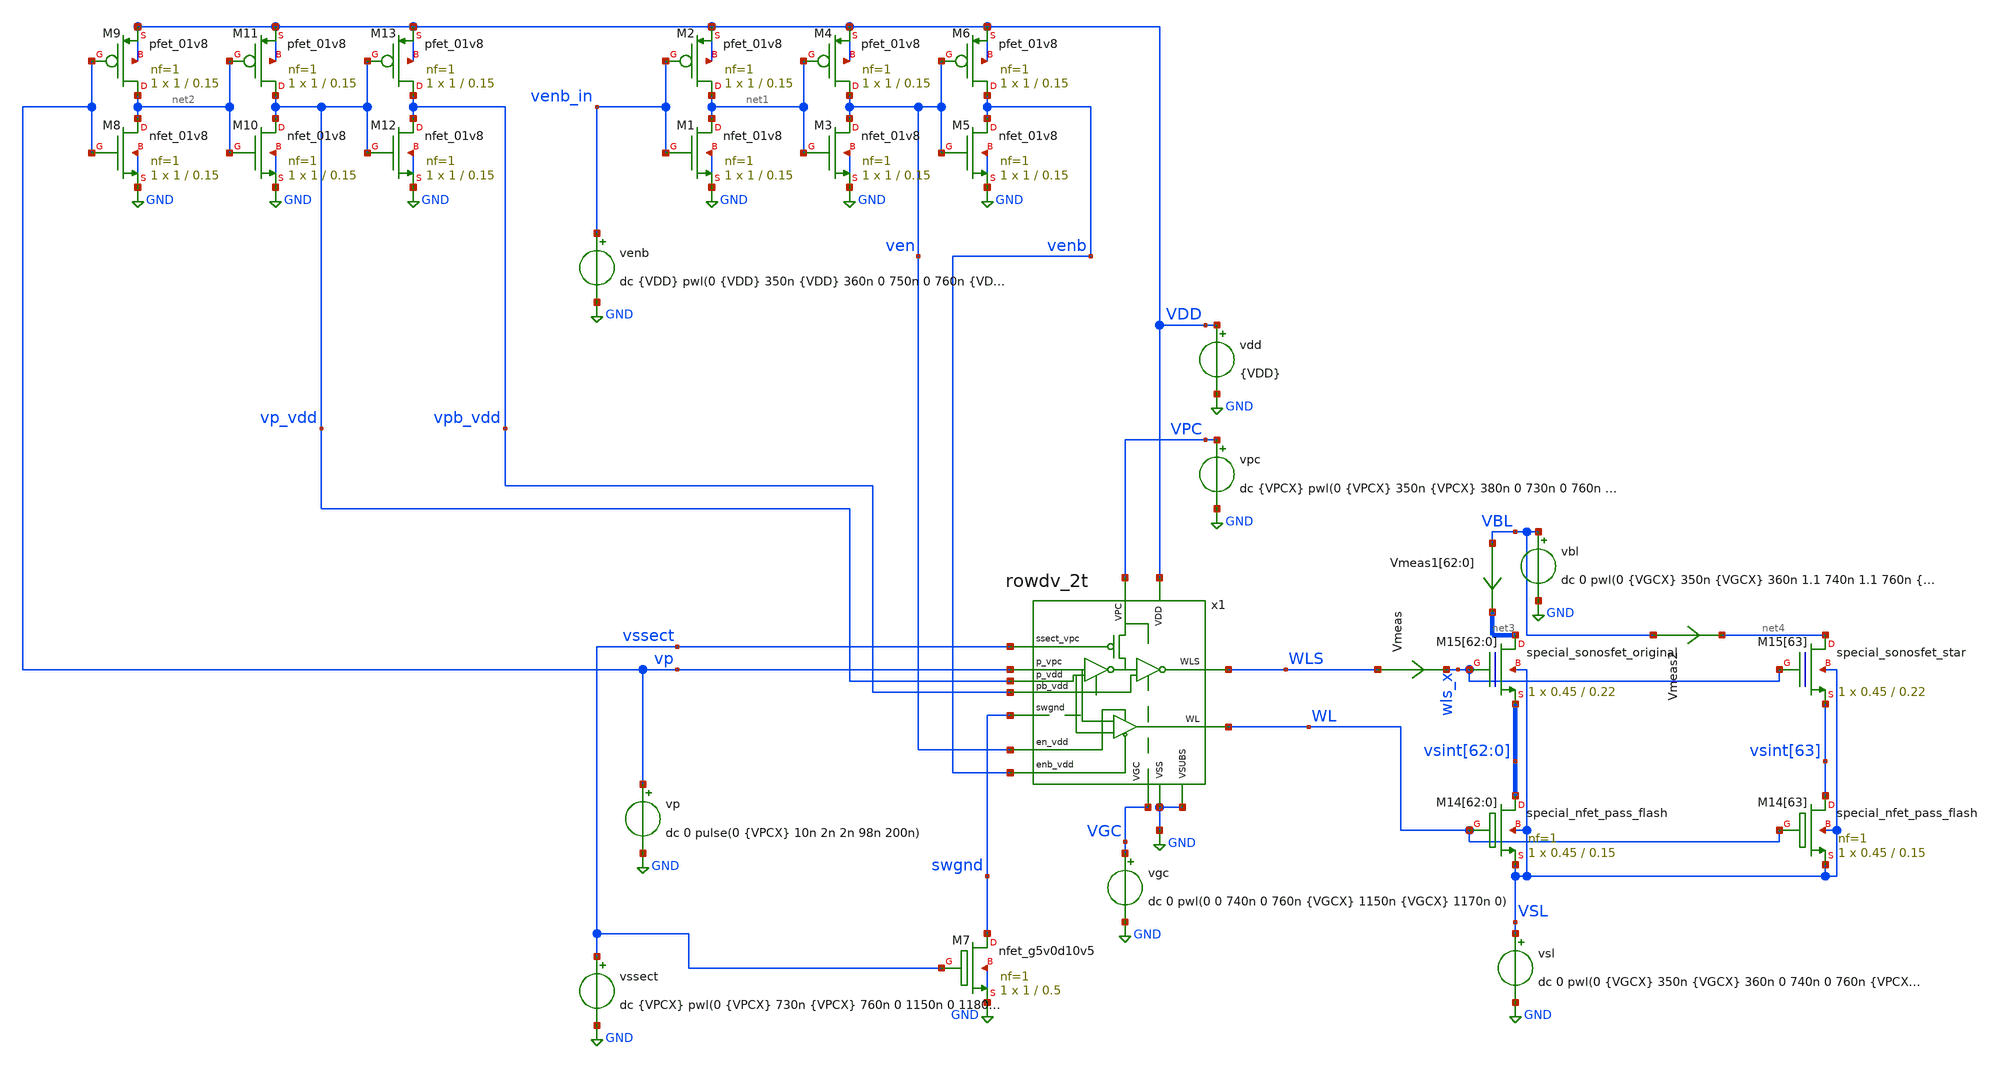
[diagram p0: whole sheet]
** sch_path: integrated/rowdv_2t_sonos/test_rowdv_2t.sch
**.subckt test_rowdv_2t
vssect vssect GND dc {VPCX} pwl(0 {VPCX} 730n {VPCX} 760n 0 1150n 0 1180n {VPCX})
vp vp GND dc 0 pulse(0 {VPCX} 10n 2n 2n 98n 200n)
venb venb_in GND dc {VDD} pwl(0 {VDD} 350n {VDD} 360n 0 750n 0 760n {VDD} 1170n {VDD} 1180n 0)
XM1 net1 venb_in GND GND sky130_fd_pr__nfet_01v8 L=0.15 W=1 nf=1 ad='int((nf+1)/2) * W/nf * 0.29' as='int((nf+2)/2) * W/nf * 0.29'
+ pd='2*int((nf+1)/2) * (W/nf + 0.29)' ps='2*int((nf+2)/2) * (W/nf + 0.29)' nrd='0.29 / W' nrs='0.29 / W'
+ sa=0 sb=0 sd=0 mult=1 m=1
XM2 net1 venb_in VDD VDD sky130_fd_pr__pfet_01v8 L=0.15 W=1 nf=1 ad='int((nf+1)/2) * W/nf * 0.29' as='int((nf+2)/2) * W/nf * 0.29'
+ pd='2*int((nf+1)/2) * (W/nf + 0.29)' ps='2*int((nf+2)/2) * (W/nf + 0.29)' nrd='0.29 / W' nrs='0.29 / W'
+ sa=0 sb=0 sd=0 mult=1 m=1
vpc VPC GND dc {VPCX} pwl(0 {VPCX} 350n {VPCX} 380n 0 730n 0 760n {VDD} 1140n {VDD} 1170n 0)
vdd VDD GND {VDD}
vgc VGC GND dc 0 pwl(0 0 740n 0 760n {VGCX} 1150n {VGCX} 1170n 0)
XM3 ven net1 GND GND sky130_fd_pr__nfet_01v8 L=0.15 W=1 nf=1 ad='int((nf+1)/2) * W/nf * 0.29' as='int((nf+2)/2) * W/nf * 0.29'
+ pd='2*int((nf+1)/2) * (W/nf + 0.29)' ps='2*int((nf+2)/2) * (W/nf + 0.29)' nrd='0.29 / W' nrs='0.29 / W'
+ sa=0 sb=0 sd=0 mult=1 m=1
XM4 ven net1 VDD VDD sky130_fd_pr__pfet_01v8 L=0.15 W=1 nf=1 ad='int((nf+1)/2) * W/nf * 0.29' as='int((nf+2)/2) * W/nf * 0.29'
+ pd='2*int((nf+1)/2) * (W/nf + 0.29)' ps='2*int((nf+2)/2) * (W/nf + 0.29)' nrd='0.29 / W' nrs='0.29 / W'
+ sa=0 sb=0 sd=0 mult=1 m=1
XM5 venb ven GND GND sky130_fd_pr__nfet_01v8 L=0.15 W=1 nf=1 ad='int((nf+1)/2) * W/nf * 0.29' as='int((nf+2)/2) * W/nf * 0.29'
+ pd='2*int((nf+1)/2) * (W/nf + 0.29)' ps='2*int((nf+2)/2) * (W/nf + 0.29)' nrd='0.29 / W' nrs='0.29 / W'
+ sa=0 sb=0 sd=0 mult=1 m=1
XM6 venb ven VDD VDD sky130_fd_pr__pfet_01v8 L=0.15 W=1 nf=1 ad='int((nf+1)/2) * W/nf * 0.29' as='int((nf+2)/2) * W/nf * 0.29'
+ pd='2*int((nf+1)/2) * (W/nf + 0.29)' ps='2*int((nf+2)/2) * (W/nf + 0.29)' nrd='0.29 / W' nrs='0.29 / W'
+ sa=0 sb=0 sd=0 mult=1 m=1
XM7 swgnd vssect GND GND sky130_fd_pr__nfet_g5v0d10v5 L=0.5 W=1 nf=1 ad='int((nf+1)/2) * W/nf * 0.29'
+ as='int((nf+2)/2) * W/nf * 0.29' pd='2*int((nf+1)/2) * (W/nf + 0.29)' ps='2*int((nf+2)/2) * (W/nf + 0.29)'
+ nrd='0.29 / W' nrs='0.29 / W' sa=0 sb=0 sd=0 mult=1 m=1
x1 vssect ven venb vp vp_vdd vpb_vdd swgnd VPC VGC VDD GND GND WLS WL rowdv_2t
XM8 net2 vp GND GND sky130_fd_pr__nfet_01v8 L=0.15 W=1 nf=1 ad='int((nf+1)/2) * W/nf * 0.29' as='int((nf+2)/2) * W/nf * 0.29'
+ pd='2*int((nf+1)/2) * (W/nf + 0.29)' ps='2*int((nf+2)/2) * (W/nf + 0.29)' nrd='0.29 / W' nrs='0.29 / W'
+ sa=0 sb=0 sd=0 mult=1 m=1
XM9 net2 vp VDD VDD sky130_fd_pr__pfet_01v8 L=0.15 W=1 nf=1 ad='int((nf+1)/2) * W/nf * 0.29' as='int((nf+2)/2) * W/nf * 0.29'
+ pd='2*int((nf+1)/2) * (W/nf + 0.29)' ps='2*int((nf+2)/2) * (W/nf + 0.29)' nrd='0.29 / W' nrs='0.29 / W'
+ sa=0 sb=0 sd=0 mult=1 m=1
XM10 vp_vdd net2 GND GND sky130_fd_pr__nfet_01v8 L=0.15 W=1 nf=1 ad='int((nf+1)/2) * W/nf * 0.29' as='int((nf+2)/2) * W/nf * 0.29'
+ pd='2*int((nf+1)/2) * (W/nf + 0.29)' ps='2*int((nf+2)/2) * (W/nf + 0.29)' nrd='0.29 / W' nrs='0.29 / W'
+ sa=0 sb=0 sd=0 mult=1 m=1
XM11 vp_vdd net2 VDD VDD sky130_fd_pr__pfet_01v8 L=0.15 W=1 nf=1 ad='int((nf+1)/2) * W/nf * 0.29' as='int((nf+2)/2) * W/nf * 0.29'
+ pd='2*int((nf+1)/2) * (W/nf + 0.29)' ps='2*int((nf+2)/2) * (W/nf + 0.29)' nrd='0.29 / W' nrs='0.29 / W'
+ sa=0 sb=0 sd=0 mult=1 m=1
XM12 vpb_vdd vp_vdd GND GND sky130_fd_pr__nfet_01v8 L=0.15 W=1 nf=1 ad='int((nf+1)/2) * W/nf * 0.29'
+ as='int((nf+2)/2) * W/nf * 0.29' pd='2*int((nf+1)/2) * (W/nf + 0.29)' ps='2*int((nf+2)/2) * (W/nf + 0.29)'
+ nrd='0.29 / W' nrs='0.29 / W' sa=0 sb=0 sd=0 mult=1 m=1
XM13 vpb_vdd vp_vdd VDD VDD sky130_fd_pr__pfet_01v8 L=0.15 W=1 nf=1 ad='int((nf+1)/2) * W/nf * 0.29'
+ as='int((nf+2)/2) * W/nf * 0.29' pd='2*int((nf+1)/2) * (W/nf + 0.29)' ps='2*int((nf+2)/2) * (W/nf + 0.29)'
+ nrd='0.29 / W' nrs='0.29 / W' sa=0 sb=0 sd=0 mult=1 m=1
XM15[62] net3[62] wls_x vsint[62] VSL sky130_fd_bs_flash__special_sonosfet_original L=0.22 W=0.45 nf=1
+ ad='1 * W * 0.29' as='1 * W * 0.29' pd='2 * (W + 0.29)' ps='2 * (W + 0.29)' nrd='0.29 / W' nrs='0.29 / W'
+ sa=0 sb=0 sd=0 mult=1 m=1
XM15[61] net3[61] wls_x vsint[61] VSL sky130_fd_bs_flash__special_sonosfet_original L=0.22 W=0.45 nf=1
+ ad='1 * W * 0.29' as='1 * W * 0.29' pd='2 * (W + 0.29)' ps='2 * (W + 0.29)' nrd='0.29 / W' nrs='0.29 / W'
+ sa=0 sb=0 sd=0 mult=1 m=1
XM15[60] net3[60] wls_x vsint[60] VSL sky130_fd_bs_flash__special_sonosfet_original L=0.22 W=0.45 nf=1
+ ad='1 * W * 0.29' as='1 * W * 0.29' pd='2 * (W + 0.29)' ps='2 * (W + 0.29)' nrd='0.29 / W' nrs='0.29 / W'
+ sa=0 sb=0 sd=0 mult=1 m=1
XM15[59] net3[59] wls_x vsint[59] VSL sky130_fd_bs_flash__special_sonosfet_original L=0.22 W=0.45 nf=1
+ ad='1 * W * 0.29' as='1 * W * 0.29' pd='2 * (W + 0.29)' ps='2 * (W + 0.29)' nrd='0.29 / W' nrs='0.29 / W'
+ sa=0 sb=0 sd=0 mult=1 m=1
XM15[58] net3[58] wls_x vsint[58] VSL sky130_fd_bs_flash__special_sonosfet_original L=0.22 W=0.45 nf=1
+ ad='1 * W * 0.29' as='1 * W * 0.29' pd='2 * (W + 0.29)' ps='2 * (W + 0.29)' nrd='0.29 / W' nrs='0.29 / W'
+ sa=0 sb=0 sd=0 mult=1 m=1
XM15[57] net3[57] wls_x vsint[57] VSL sky130_fd_bs_flash__special_sonosfet_original L=0.22 W=0.45 nf=1
+ ad='1 * W * 0.29' as='1 * W * 0.29' pd='2 * (W + 0.29)' ps='2 * (W + 0.29)' nrd='0.29 / W' nrs='0.29 / W'
+ sa=0 sb=0 sd=0 mult=1 m=1
XM15[56] net3[56] wls_x vsint[56] VSL sky130_fd_bs_flash__special_sonosfet_original L=0.22 W=0.45 nf=1
+ ad='1 * W * 0.29' as='1 * W * 0.29' pd='2 * (W + 0.29)' ps='2 * (W + 0.29)' nrd='0.29 / W' nrs='0.29 / W'
+ sa=0 sb=0 sd=0 mult=1 m=1
XM15[55] net3[55] wls_x vsint[55] VSL sky130_fd_bs_flash__special_sonosfet_original L=0.22 W=0.45 nf=1
+ ad='1 * W * 0.29' as='1 * W * 0.29' pd='2 * (W + 0.29)' ps='2 * (W + 0.29)' nrd='0.29 / W' nrs='0.29 / W'
+ sa=0 sb=0 sd=0 mult=1 m=1
XM15[54] net3[54] wls_x vsint[54] VSL sky130_fd_bs_flash__special_sonosfet_original L=0.22 W=0.45 nf=1
+ ad='1 * W * 0.29' as='1 * W * 0.29' pd='2 * (W + 0.29)' ps='2 * (W + 0.29)' nrd='0.29 / W' nrs='0.29 / W'
+ sa=0 sb=0 sd=0 mult=1 m=1
XM15[53] net3[53] wls_x vsint[53] VSL sky130_fd_bs_flash__special_sonosfet_original L=0.22 W=0.45 nf=1
+ ad='1 * W * 0.29' as='1 * W * 0.29' pd='2 * (W + 0.29)' ps='2 * (W + 0.29)' nrd='0.29 / W' nrs='0.29 / W'
+ sa=0 sb=0 sd=0 mult=1 m=1
XM15[52] net3[52] wls_x vsint[52] VSL sky130_fd_bs_flash__special_sonosfet_original L=0.22 W=0.45 nf=1
+ ad='1 * W * 0.29' as='1 * W * 0.29' pd='2 * (W + 0.29)' ps='2 * (W + 0.29)' nrd='0.29 / W' nrs='0.29 / W'
+ sa=0 sb=0 sd=0 mult=1 m=1
XM15[51] net3[51] wls_x vsint[51] VSL sky130_fd_bs_flash__special_sonosfet_original L=0.22 W=0.45 nf=1
+ ad='1 * W * 0.29' as='1 * W * 0.29' pd='2 * (W + 0.29)' ps='2 * (W + 0.29)' nrd='0.29 / W' nrs='0.29 / W'
+ sa=0 sb=0 sd=0 mult=1 m=1
XM15[50] net3[50] wls_x vsint[50] VSL sky130_fd_bs_flash__special_sonosfet_original L=0.22 W=0.45 nf=1
+ ad='1 * W * 0.29' as='1 * W * 0.29' pd='2 * (W + 0.29)' ps='2 * (W + 0.29)' nrd='0.29 / W' nrs='0.29 / W'
+ sa=0 sb=0 sd=0 mult=1 m=1
XM15[49] net3[49] wls_x vsint[49] VSL sky130_fd_bs_flash__special_sonosfet_original L=0.22 W=0.45 nf=1
+ ad='1 * W * 0.29' as='1 * W * 0.29' pd='2 * (W + 0.29)' ps='2 * (W + 0.29)' nrd='0.29 / W' nrs='0.29 / W'
+ sa=0 sb=0 sd=0 mult=1 m=1
XM15[48] net3[48] wls_x vsint[48] VSL sky130_fd_bs_flash__special_sonosfet_original L=0.22 W=0.45 nf=1
+ ad='1 * W * 0.29' as='1 * W * 0.29' pd='2 * (W + 0.29)' ps='2 * (W + 0.29)' nrd='0.29 / W' nrs='0.29 / W'
+ sa=0 sb=0 sd=0 mult=1 m=1
XM15[47] net3[47] wls_x vsint[47] VSL sky130_fd_bs_flash__special_sonosfet_original L=0.22 W=0.45 nf=1
+ ad='1 * W * 0.29' as='1 * W * 0.29' pd='2 * (W + 0.29)' ps='2 * (W + 0.29)' nrd='0.29 / W' nrs='0.29 / W'
+ sa=0 sb=0 sd=0 mult=1 m=1
XM15[46] net3[46] wls_x vsint[46] VSL sky130_fd_bs_flash__special_sonosfet_original L=0.22 W=0.45 nf=1
+ ad='1 * W * 0.29' as='1 * W * 0.29' pd='2 * (W + 0.29)' ps='2 * (W + 0.29)' nrd='0.29 / W' nrs='0.29 / W'
+ sa=0 sb=0 sd=0 mult=1 m=1
XM15[45] net3[45] wls_x vsint[45] VSL sky130_fd_bs_flash__special_sonosfet_original L=0.22 W=0.45 nf=1
+ ad='1 * W * 0.29' as='1 * W * 0.29' pd='2 * (W + 0.29)' ps='2 * (W + 0.29)' nrd='0.29 / W' nrs='0.29 / W'
+ sa=0 sb=0 sd=0 mult=1 m=1
XM15[44] net3[44] wls_x vsint[44] VSL sky130_fd_bs_flash__special_sonosfet_original L=0.22 W=0.45 nf=1
+ ad='1 * W * 0.29' as='1 * W * 0.29' pd='2 * (W + 0.29)' ps='2 * (W + 0.29)' nrd='0.29 / W' nrs='0.29 / W'
+ sa=0 sb=0 sd=0 mult=1 m=1
XM15[43] net3[43] wls_x vsint[43] VSL sky130_fd_bs_flash__special_sonosfet_original L=0.22 W=0.45 nf=1
+ ad='1 * W * 0.29' as='1 * W * 0.29' pd='2 * (W + 0.29)' ps='2 * (W + 0.29)' nrd='0.29 / W' nrs='0.29 / W'
+ sa=0 sb=0 sd=0 mult=1 m=1
XM15[42] net3[42] wls_x vsint[42] VSL sky130_fd_bs_flash__special_sonosfet_original L=0.22 W=0.45 nf=1
+ ad='1 * W * 0.29' as='1 * W * 0.29' pd='2 * (W + 0.29)' ps='2 * (W + 0.29)' nrd='0.29 / W' nrs='0.29 / W'
+ sa=0 sb=0 sd=0 mult=1 m=1
XM15[41] net3[41] wls_x vsint[41] VSL sky130_fd_bs_flash__special_sonosfet_original L=0.22 W=0.45 nf=1
+ ad='1 * W * 0.29' as='1 * W * 0.29' pd='2 * (W + 0.29)' ps='2 * (W + 0.29)' nrd='0.29 / W' nrs='0.29 / W'
+ sa=0 sb=0 sd=0 mult=1 m=1
XM15[40] net3[40] wls_x vsint[40] VSL sky130_fd_bs_flash__special_sonosfet_original L=0.22 W=0.45 nf=1
+ ad='1 * W * 0.29' as='1 * W * 0.29' pd='2 * (W + 0.29)' ps='2 * (W + 0.29)' nrd='0.29 / W' nrs='0.29 / W'
+ sa=0 sb=0 sd=0 mult=1 m=1
XM15[39] net3[39] wls_x vsint[39] VSL sky130_fd_bs_flash__special_sonosfet_original L=0.22 W=0.45 nf=1
+ ad='1 * W * 0.29' as='1 * W * 0.29' pd='2 * (W + 0.29)' ps='2 * (W + 0.29)' nrd='0.29 / W' nrs='0.29 / W'
+ sa=0 sb=0 sd=0 mult=1 m=1
XM15[38] net3[38] wls_x vsint[38] VSL sky130_fd_bs_flash__special_sonosfet_original L=0.22 W=0.45 nf=1
+ ad='1 * W * 0.29' as='1 * W * 0.29' pd='2 * (W + 0.29)' ps='2 * (W + 0.29)' nrd='0.29 / W' nrs='0.29 / W'
+ sa=0 sb=0 sd=0 mult=1 m=1
XM15[37] net3[37] wls_x vsint[37] VSL sky130_fd_bs_flash__special_sonosfet_original L=0.22 W=0.45 nf=1
+ ad='1 * W * 0.29' as='1 * W * 0.29' pd='2 * (W + 0.29)' ps='2 * (W + 0.29)' nrd='0.29 / W' nrs='0.29 / W'
+ sa=0 sb=0 sd=0 mult=1 m=1
XM15[36] net3[36] wls_x vsint[36] VSL sky130_fd_bs_flash__special_sonosfet_original L=0.22 W=0.45 nf=1
+ ad='1 * W * 0.29' as='1 * W * 0.29' pd='2 * (W + 0.29)' ps='2 * (W + 0.29)' nrd='0.29 / W' nrs='0.29 / W'
+ sa=0 sb=0 sd=0 mult=1 m=1
XM15[35] net3[35] wls_x vsint[35] VSL sky130_fd_bs_flash__special_sonosfet_original L=0.22 W=0.45 nf=1
+ ad='1 * W * 0.29' as='1 * W * 0.29' pd='2 * (W + 0.29)' ps='2 * (W + 0.29)' nrd='0.29 / W' nrs='0.29 / W'
+ sa=0 sb=0 sd=0 mult=1 m=1
XM15[34] net3[34] wls_x vsint[34] VSL sky130_fd_bs_flash__special_sonosfet_original L=0.22 W=0.45 nf=1
+ ad='1 * W * 0.29' as='1 * W * 0.29' pd='2 * (W + 0.29)' ps='2 * (W + 0.29)' nrd='0.29 / W' nrs='0.29 / W'
+ sa=0 sb=0 sd=0 mult=1 m=1
XM15[33] net3[33] wls_x vsint[33] VSL sky130_fd_bs_flash__special_sonosfet_original L=0.22 W=0.45 nf=1
+ ad='1 * W * 0.29' as='1 * W * 0.29' pd='2 * (W + 0.29)' ps='2 * (W + 0.29)' nrd='0.29 / W' nrs='0.29 / W'
+ sa=0 sb=0 sd=0 mult=1 m=1
XM15[32] net3[32] wls_x vsint[32] VSL sky130_fd_bs_flash__special_sonosfet_original L=0.22 W=0.45 nf=1
+ ad='1 * W * 0.29' as='1 * W * 0.29' pd='2 * (W + 0.29)' ps='2 * (W + 0.29)' nrd='0.29 / W' nrs='0.29 / W'
+ sa=0 sb=0 sd=0 mult=1 m=1
XM15[31] net3[31] wls_x vsint[31] VSL sky130_fd_bs_flash__special_sonosfet_original L=0.22 W=0.45 nf=1
+ ad='1 * W * 0.29' as='1 * W * 0.29' pd='2 * (W + 0.29)' ps='2 * (W + 0.29)' nrd='0.29 / W' nrs='0.29 / W'
+ sa=0 sb=0 sd=0 mult=1 m=1
XM15[30] net3[30] wls_x vsint[30] VSL sky130_fd_bs_flash__special_sonosfet_original L=0.22 W=0.45 nf=1
+ ad='1 * W * 0.29' as='1 * W * 0.29' pd='2 * (W + 0.29)' ps='2 * (W + 0.29)' nrd='0.29 / W' nrs='0.29 / W'
+ sa=0 sb=0 sd=0 mult=1 m=1
XM15[29] net3[29] wls_x vsint[29] VSL sky130_fd_bs_flash__special_sonosfet_original L=0.22 W=0.45 nf=1
+ ad='1 * W * 0.29' as='1 * W * 0.29' pd='2 * (W + 0.29)' ps='2 * (W + 0.29)' nrd='0.29 / W' nrs='0.29 / W'
+ sa=0 sb=0 sd=0 mult=1 m=1
XM15[28] net3[28] wls_x vsint[28] VSL sky130_fd_bs_flash__special_sonosfet_original L=0.22 W=0.45 nf=1
+ ad='1 * W * 0.29' as='1 * W * 0.29' pd='2 * (W + 0.29)' ps='2 * (W + 0.29)' nrd='0.29 / W' nrs='0.29 / W'
+ sa=0 sb=0 sd=0 mult=1 m=1
XM15[27] net3[27] wls_x vsint[27] VSL sky130_fd_bs_flash__special_sonosfet_original L=0.22 W=0.45 nf=1
+ ad='1 * W * 0.29' as='1 * W * 0.29' pd='2 * (W + 0.29)' ps='2 * (W + 0.29)' nrd='0.29 / W' nrs='0.29 / W'
+ sa=0 sb=0 sd=0 mult=1 m=1
XM15[26] net3[26] wls_x vsint[26] VSL sky130_fd_bs_flash__special_sonosfet_original L=0.22 W=0.45 nf=1
+ ad='1 * W * 0.29' as='1 * W * 0.29' pd='2 * (W + 0.29)' ps='2 * (W + 0.29)' nrd='0.29 / W' nrs='0.29 / W'
+ sa=0 sb=0 sd=0 mult=1 m=1
XM15[25] net3[25] wls_x vsint[25] VSL sky130_fd_bs_flash__special_sonosfet_original L=0.22 W=0.45 nf=1
+ ad='1 * W * 0.29' as='1 * W * 0.29' pd='2 * (W + 0.29)' ps='2 * (W + 0.29)' nrd='0.29 / W' nrs='0.29 / W'
+ sa=0 sb=0 sd=0 mult=1 m=1
XM15[24] net3[24] wls_x vsint[24] VSL sky130_fd_bs_flash__special_sonosfet_original L=0.22 W=0.45 nf=1
+ ad='1 * W * 0.29' as='1 * W * 0.29' pd='2 * (W + 0.29)' ps='2 * (W + 0.29)' nrd='0.29 / W' nrs='0.29 / W'
+ sa=0 sb=0 sd=0 mult=1 m=1
XM15[23] net3[23] wls_x vsint[23] VSL sky130_fd_bs_flash__special_sonosfet_original L=0.22 W=0.45 nf=1
+ ad='1 * W * 0.29' as='1 * W * 0.29' pd='2 * (W + 0.29)' ps='2 * (W + 0.29)' nrd='0.29 / W' nrs='0.29 / W'
+ sa=0 sb=0 sd=0 mult=1 m=1
XM15[22] net3[22] wls_x vsint[22] VSL sky130_fd_bs_flash__special_sonosfet_original L=0.22 W=0.45 nf=1
+ ad='1 * W * 0.29' as='1 * W * 0.29' pd='2 * (W + 0.29)' ps='2 * (W + 0.29)' nrd='0.29 / W' nrs='0.29 / W'
+ sa=0 sb=0 sd=0 mult=1 m=1
XM15[21] net3[21] wls_x vsint[21] VSL sky130_fd_bs_flash__special_sonosfet_original L=0.22 W=0.45 nf=1
+ ad='1 * W * 0.29' as='1 * W * 0.29' pd='2 * (W + 0.29)' ps='2 * (W + 0.29)' nrd='0.29 / W' nrs='0.29 / W'
+ sa=0 sb=0 sd=0 mult=1 m=1
XM15[20] net3[20] wls_x vsint[20] VSL sky130_fd_bs_flash__special_sonosfet_original L=0.22 W=0.45 nf=1
+ ad='1 * W * 0.29' as='1 * W * 0.29' pd='2 * (W + 0.29)' ps='2 * (W + 0.29)' nrd='0.29 / W' nrs='0.29 / W'
+ sa=0 sb=0 sd=0 mult=1 m=1
XM15[19] net3[19] wls_x vsint[19] VSL sky130_fd_bs_flash__special_sonosfet_original L=0.22 W=0.45 nf=1
+ ad='1 * W * 0.29' as='1 * W * 0.29' pd='2 * (W + 0.29)' ps='2 * (W + 0.29)' nrd='0.29 / W' nrs='0.29 / W'
+ sa=0 sb=0 sd=0 mult=1 m=1
XM15[18] net3[18] wls_x vsint[18] VSL sky130_fd_bs_flash__special_sonosfet_original L=0.22 W=0.45 nf=1
+ ad='1 * W * 0.29' as='1 * W * 0.29' pd='2 * (W + 0.29)' ps='2 * (W + 0.29)' nrd='0.29 / W' nrs='0.29 / W'
+ sa=0 sb=0 sd=0 mult=1 m=1
XM15[17] net3[17] wls_x vsint[17] VSL sky130_fd_bs_flash__special_sonosfet_original L=0.22 W=0.45 nf=1
+ ad='1 * W * 0.29' as='1 * W * 0.29' pd='2 * (W + 0.29)' ps='2 * (W + 0.29)' nrd='0.29 / W' nrs='0.29 / W'
+ sa=0 sb=0 sd=0 mult=1 m=1
XM15[16] net3[16] wls_x vsint[16] VSL sky130_fd_bs_flash__special_sonosfet_original L=0.22 W=0.45 nf=1
+ ad='1 * W * 0.29' as='1 * W * 0.29' pd='2 * (W + 0.29)' ps='2 * (W + 0.29)' nrd='0.29 / W' nrs='0.29 / W'
+ sa=0 sb=0 sd=0 mult=1 m=1
XM15[15] net3[15] wls_x vsint[15] VSL sky130_fd_bs_flash__special_sonosfet_original L=0.22 W=0.45 nf=1
+ ad='1 * W * 0.29' as='1 * W * 0.29' pd='2 * (W + 0.29)' ps='2 * (W + 0.29)' nrd='0.29 / W' nrs='0.29 / W'
+ sa=0 sb=0 sd=0 mult=1 m=1
XM15[14] net3[14] wls_x vsint[14] VSL sky130_fd_bs_flash__special_sonosfet_original L=0.22 W=0.45 nf=1
+ ad='1 * W * 0.29' as='1 * W * 0.29' pd='2 * (W + 0.29)' ps='2 * (W + 0.29)' nrd='0.29 / W' nrs='0.29 / W'
+ sa=0 sb=0 sd=0 mult=1 m=1
XM15[13] net3[13] wls_x vsint[13] VSL sky130_fd_bs_flash__special_sonosfet_original L=0.22 W=0.45 nf=1
+ ad='1 * W * 0.29' as='1 * W * 0.29' pd='2 * (W + 0.29)' ps='2 * (W + 0.29)' nrd='0.29 / W' nrs='0.29 / W'
+ sa=0 sb=0 sd=0 mult=1 m=1
XM15[12] net3[12] wls_x vsint[12] VSL sky130_fd_bs_flash__special_sonosfet_original L=0.22 W=0.45 nf=1
+ ad='1 * W * 0.29' as='1 * W * 0.29' pd='2 * (W + 0.29)' ps='2 * (W + 0.29)' nrd='0.29 / W' nrs='0.29 / W'
+ sa=0 sb=0 sd=0 mult=1 m=1
XM15[11] net3[11] wls_x vsint[11] VSL sky130_fd_bs_flash__special_sonosfet_original L=0.22 W=0.45 nf=1
+ ad='1 * W * 0.29' as='1 * W * 0.29' pd='2 * (W + 0.29)' ps='2 * (W + 0.29)' nrd='0.29 / W' nrs='0.29 / W'
+ sa=0 sb=0 sd=0 mult=1 m=1
XM15[10] net3[10] wls_x vsint[10] VSL sky130_fd_bs_flash__special_sonosfet_original L=0.22 W=0.45 nf=1
+ ad='1 * W * 0.29' as='1 * W * 0.29' pd='2 * (W + 0.29)' ps='2 * (W + 0.29)' nrd='0.29 / W' nrs='0.29 / W'
+ sa=0 sb=0 sd=0 mult=1 m=1
XM15[9] net3[9] wls_x vsint[9] VSL sky130_fd_bs_flash__special_sonosfet_original L=0.22 W=0.45 nf=1 ad='1 * W * 0.29'
+ as='1 * W * 0.29' pd='2 * (W + 0.29)' ps='2 * (W + 0.29)' nrd='0.29 / W' nrs='0.29 / W' sa=0 sb=0 sd=0
+ mult=1 m=1
XM15[8] net3[8] wls_x vsint[8] VSL sky130_fd_bs_flash__special_sonosfet_original L=0.22 W=0.45 nf=1 ad='1 * W * 0.29'
+ as='1 * W * 0.29' pd='2 * (W + 0.29)' ps='2 * (W + 0.29)' nrd='0.29 / W' nrs='0.29 / W' sa=0 sb=0 sd=0
+ mult=1 m=1
XM15[7] net3[7] wls_x vsint[7] VSL sky130_fd_bs_flash__special_sonosfet_original L=0.22 W=0.45 nf=1 ad='1 * W * 0.29'
+ as='1 * W * 0.29' pd='2 * (W + 0.29)' ps='2 * (W + 0.29)' nrd='0.29 / W' nrs='0.29 / W' sa=0 sb=0 sd=0
+ mult=1 m=1
XM15[6] net3[6] wls_x vsint[6] VSL sky130_fd_bs_flash__special_sonosfet_original L=0.22 W=0.45 nf=1 ad='1 * W * 0.29'
+ as='1 * W * 0.29' pd='2 * (W + 0.29)' ps='2 * (W + 0.29)' nrd='0.29 / W' nrs='0.29 / W' sa=0 sb=0 sd=0
+ mult=1 m=1
XM15[5] net3[5] wls_x vsint[5] VSL sky130_fd_bs_flash__special_sonosfet_original L=0.22 W=0.45 nf=1 ad='1 * W * 0.29'
+ as='1 * W * 0.29' pd='2 * (W + 0.29)' ps='2 * (W + 0.29)' nrd='0.29 / W' nrs='0.29 / W' sa=0 sb=0 sd=0
+ mult=1 m=1
XM15[4] net3[4] wls_x vsint[4] VSL sky130_fd_bs_flash__special_sonosfet_original L=0.22 W=0.45 nf=1 ad='1 * W * 0.29'
+ as='1 * W * 0.29' pd='2 * (W + 0.29)' ps='2 * (W + 0.29)' nrd='0.29 / W' nrs='0.29 / W' sa=0 sb=0 sd=0
+ mult=1 m=1
XM15[3] net3[3] wls_x vsint[3] VSL sky130_fd_bs_flash__special_sonosfet_original L=0.22 W=0.45 nf=1 ad='1 * W * 0.29'
+ as='1 * W * 0.29' pd='2 * (W + 0.29)' ps='2 * (W + 0.29)' nrd='0.29 / W' nrs='0.29 / W' sa=0 sb=0 sd=0
+ mult=1 m=1
XM15[2] net3[2] wls_x vsint[2] VSL sky130_fd_bs_flash__special_sonosfet_original L=0.22 W=0.45 nf=1 ad='1 * W * 0.29'
+ as='1 * W * 0.29' pd='2 * (W + 0.29)' ps='2 * (W + 0.29)' nrd='0.29 / W' nrs='0.29 / W' sa=0 sb=0 sd=0
+ mult=1 m=1
XM15[1] net3[1] wls_x vsint[1] VSL sky130_fd_bs_flash__special_sonosfet_original L=0.22 W=0.45 nf=1 ad='1 * W * 0.29'
+ as='1 * W * 0.29' pd='2 * (W + 0.29)' ps='2 * (W + 0.29)' nrd='0.29 / W' nrs='0.29 / W' sa=0 sb=0 sd=0
+ mult=1 m=1
XM15[0] net3[0] wls_x vsint[0] VSL sky130_fd_bs_flash__special_sonosfet_original L=0.22 W=0.45 nf=1 ad='1 * W * 0.29'
+ as='1 * W * 0.29' pd='2 * (W + 0.29)' ps='2 * (W + 0.29)' nrd='0.29 / W' nrs='0.29 / W' sa=0 sb=0 sd=0
+ mult=1 m=1
vbl VBL GND dc 0 pwl(0 {VGCX} 350n {VGCX} 360n 1.1 740n 1.1 760n {VPCX} 1170n {VPCX} 1190n 1.1)
vsl VSL GND dc 0 pwl(0 {VGCX} 350n {VGCX} 360n 0 740n 0 760n {VPCX} 1170n {VPCX} 1190n 0)
Vmeas WLS wls_x 0
.save i(vmeas)
XM14[62] vsint[62] WL VSL VSL sky130_fd_pr__special_nfet_pass_flash L=0.15 W=0.45 nf=1 ad='1 * W * 0.29'
+ as='1 * W * 0.29' pd='2 * (W + 0.29)' ps='2 * (W + 0.29)' nrd='0.29 / W' nrs='0.29 / W' sa=0 sb=0 sd=0
+ mult=1 m=1
XM14[61] vsint[61] WL VSL VSL sky130_fd_pr__special_nfet_pass_flash L=0.15 W=0.45 nf=1 ad='1 * W * 0.29'
+ as='1 * W * 0.29' pd='2 * (W + 0.29)' ps='2 * (W + 0.29)' nrd='0.29 / W' nrs='0.29 / W' sa=0 sb=0 sd=0
+ mult=1 m=1
XM14[60] vsint[60] WL VSL VSL sky130_fd_pr__special_nfet_pass_flash L=0.15 W=0.45 nf=1 ad='1 * W * 0.29'
+ as='1 * W * 0.29' pd='2 * (W + 0.29)' ps='2 * (W + 0.29)' nrd='0.29 / W' nrs='0.29 / W' sa=0 sb=0 sd=0
+ mult=1 m=1
XM14[59] vsint[59] WL VSL VSL sky130_fd_pr__special_nfet_pass_flash L=0.15 W=0.45 nf=1 ad='1 * W * 0.29'
+ as='1 * W * 0.29' pd='2 * (W + 0.29)' ps='2 * (W + 0.29)' nrd='0.29 / W' nrs='0.29 / W' sa=0 sb=0 sd=0
+ mult=1 m=1
XM14[58] vsint[58] WL VSL VSL sky130_fd_pr__special_nfet_pass_flash L=0.15 W=0.45 nf=1 ad='1 * W * 0.29'
+ as='1 * W * 0.29' pd='2 * (W + 0.29)' ps='2 * (W + 0.29)' nrd='0.29 / W' nrs='0.29 / W' sa=0 sb=0 sd=0
+ mult=1 m=1
XM14[57] vsint[57] WL VSL VSL sky130_fd_pr__special_nfet_pass_flash L=0.15 W=0.45 nf=1 ad='1 * W * 0.29'
+ as='1 * W * 0.29' pd='2 * (W + 0.29)' ps='2 * (W + 0.29)' nrd='0.29 / W' nrs='0.29 / W' sa=0 sb=0 sd=0
+ mult=1 m=1
XM14[56] vsint[56] WL VSL VSL sky130_fd_pr__special_nfet_pass_flash L=0.15 W=0.45 nf=1 ad='1 * W * 0.29'
+ as='1 * W * 0.29' pd='2 * (W + 0.29)' ps='2 * (W + 0.29)' nrd='0.29 / W' nrs='0.29 / W' sa=0 sb=0 sd=0
+ mult=1 m=1
XM14[55] vsint[55] WL VSL VSL sky130_fd_pr__special_nfet_pass_flash L=0.15 W=0.45 nf=1 ad='1 * W * 0.29'
+ as='1 * W * 0.29' pd='2 * (W + 0.29)' ps='2 * (W + 0.29)' nrd='0.29 / W' nrs='0.29 / W' sa=0 sb=0 sd=0
+ mult=1 m=1
XM14[54] vsint[54] WL VSL VSL sky130_fd_pr__special_nfet_pass_flash L=0.15 W=0.45 nf=1 ad='1 * W * 0.29'
+ as='1 * W * 0.29' pd='2 * (W + 0.29)' ps='2 * (W + 0.29)' nrd='0.29 / W' nrs='0.29 / W' sa=0 sb=0 sd=0
+ mult=1 m=1
XM14[53] vsint[53] WL VSL VSL sky130_fd_pr__special_nfet_pass_flash L=0.15 W=0.45 nf=1 ad='1 * W * 0.29'
+ as='1 * W * 0.29' pd='2 * (W + 0.29)' ps='2 * (W + 0.29)' nrd='0.29 / W' nrs='0.29 / W' sa=0 sb=0 sd=0
+ mult=1 m=1
XM14[52] vsint[52] WL VSL VSL sky130_fd_pr__special_nfet_pass_flash L=0.15 W=0.45 nf=1 ad='1 * W * 0.29'
+ as='1 * W * 0.29' pd='2 * (W + 0.29)' ps='2 * (W + 0.29)' nrd='0.29 / W' nrs='0.29 / W' sa=0 sb=0 sd=0
+ mult=1 m=1
XM14[51] vsint[51] WL VSL VSL sky130_fd_pr__special_nfet_pass_flash L=0.15 W=0.45 nf=1 ad='1 * W * 0.29'
+ as='1 * W * 0.29' pd='2 * (W + 0.29)' ps='2 * (W + 0.29)' nrd='0.29 / W' nrs='0.29 / W' sa=0 sb=0 sd=0
+ mult=1 m=1
XM14[50] vsint[50] WL VSL VSL sky130_fd_pr__special_nfet_pass_flash L=0.15 W=0.45 nf=1 ad='1 * W * 0.29'
+ as='1 * W * 0.29' pd='2 * (W + 0.29)' ps='2 * (W + 0.29)' nrd='0.29 / W' nrs='0.29 / W' sa=0 sb=0 sd=0
+ mult=1 m=1
XM14[49] vsint[49] WL VSL VSL sky130_fd_pr__special_nfet_pass_flash L=0.15 W=0.45 nf=1 ad='1 * W * 0.29'
+ as='1 * W * 0.29' pd='2 * (W + 0.29)' ps='2 * (W + 0.29)' nrd='0.29 / W' nrs='0.29 / W' sa=0 sb=0 sd=0
+ mult=1 m=1
XM14[48] vsint[48] WL VSL VSL sky130_fd_pr__special_nfet_pass_flash L=0.15 W=0.45 nf=1 ad='1 * W * 0.29'
+ as='1 * W * 0.29' pd='2 * (W + 0.29)' ps='2 * (W + 0.29)' nrd='0.29 / W' nrs='0.29 / W' sa=0 sb=0 sd=0
+ mult=1 m=1
XM14[47] vsint[47] WL VSL VSL sky130_fd_pr__special_nfet_pass_flash L=0.15 W=0.45 nf=1 ad='1 * W * 0.29'
+ as='1 * W * 0.29' pd='2 * (W + 0.29)' ps='2 * (W + 0.29)' nrd='0.29 / W' nrs='0.29 / W' sa=0 sb=0 sd=0
+ mult=1 m=1
XM14[46] vsint[46] WL VSL VSL sky130_fd_pr__special_nfet_pass_flash L=0.15 W=0.45 nf=1 ad='1 * W * 0.29'
+ as='1 * W * 0.29' pd='2 * (W + 0.29)' ps='2 * (W + 0.29)' nrd='0.29 / W' nrs='0.29 / W' sa=0 sb=0 sd=0
+ mult=1 m=1
XM14[45] vsint[45] WL VSL VSL sky130_fd_pr__special_nfet_pass_flash L=0.15 W=0.45 nf=1 ad='1 * W * 0.29'
+ as='1 * W * 0.29' pd='2 * (W + 0.29)' ps='2 * (W + 0.29)' nrd='0.29 / W' nrs='0.29 / W' sa=0 sb=0 sd=0
+ mult=1 m=1
XM14[44] vsint[44] WL VSL VSL sky130_fd_pr__special_nfet_pass_flash L=0.15 W=0.45 nf=1 ad='1 * W * 0.29'
+ as='1 * W * 0.29' pd='2 * (W + 0.29)' ps='2 * (W + 0.29)' nrd='0.29 / W' nrs='0.29 / W' sa=0 sb=0 sd=0
+ mult=1 m=1
XM14[43] vsint[43] WL VSL VSL sky130_fd_pr__special_nfet_pass_flash L=0.15 W=0.45 nf=1 ad='1 * W * 0.29'
+ as='1 * W * 0.29' pd='2 * (W + 0.29)' ps='2 * (W + 0.29)' nrd='0.29 / W' nrs='0.29 / W' sa=0 sb=0 sd=0
+ mult=1 m=1
XM14[42] vsint[42] WL VSL VSL sky130_fd_pr__special_nfet_pass_flash L=0.15 W=0.45 nf=1 ad='1 * W * 0.29'
+ as='1 * W * 0.29' pd='2 * (W + 0.29)' ps='2 * (W + 0.29)' nrd='0.29 / W' nrs='0.29 / W' sa=0 sb=0 sd=0
+ mult=1 m=1
XM14[41] vsint[41] WL VSL VSL sky130_fd_pr__special_nfet_pass_flash L=0.15 W=0.45 nf=1 ad='1 * W * 0.29'
+ as='1 * W * 0.29' pd='2 * (W + 0.29)' ps='2 * (W + 0.29)' nrd='0.29 / W' nrs='0.29 / W' sa=0 sb=0 sd=0
+ mult=1 m=1
XM14[40] vsint[40] WL VSL VSL sky130_fd_pr__special_nfet_pass_flash L=0.15 W=0.45 nf=1 ad='1 * W * 0.29'
+ as='1 * W * 0.29' pd='2 * (W + 0.29)' ps='2 * (W + 0.29)' nrd='0.29 / W' nrs='0.29 / W' sa=0 sb=0 sd=0
+ mult=1 m=1
XM14[39] vsint[39] WL VSL VSL sky130_fd_pr__special_nfet_pass_flash L=0.15 W=0.45 nf=1 ad='1 * W * 0.29'
+ as='1 * W * 0.29' pd='2 * (W + 0.29)' ps='2 * (W + 0.29)' nrd='0.29 / W' nrs='0.29 / W' sa=0 sb=0 sd=0
+ mult=1 m=1
XM14[38] vsint[38] WL VSL VSL sky130_fd_pr__special_nfet_pass_flash L=0.15 W=0.45 nf=1 ad='1 * W * 0.29'
+ as='1 * W * 0.29' pd='2 * (W + 0.29)' ps='2 * (W + 0.29)' nrd='0.29 / W' nrs='0.29 / W' sa=0 sb=0 sd=0
+ mult=1 m=1
XM14[37] vsint[37] WL VSL VSL sky130_fd_pr__special_nfet_pass_flash L=0.15 W=0.45 nf=1 ad='1 * W * 0.29'
+ as='1 * W * 0.29' pd='2 * (W + 0.29)' ps='2 * (W + 0.29)' nrd='0.29 / W' nrs='0.29 / W' sa=0 sb=0 sd=0
+ mult=1 m=1
XM14[36] vsint[36] WL VSL VSL sky130_fd_pr__special_nfet_pass_flash L=0.15 W=0.45 nf=1 ad='1 * W * 0.29'
+ as='1 * W * 0.29' pd='2 * (W + 0.29)' ps='2 * (W + 0.29)' nrd='0.29 / W' nrs='0.29 / W' sa=0 sb=0 sd=0
+ mult=1 m=1
XM14[35] vsint[35] WL VSL VSL sky130_fd_pr__special_nfet_pass_flash L=0.15 W=0.45 nf=1 ad='1 * W * 0.29'
+ as='1 * W * 0.29' pd='2 * (W + 0.29)' ps='2 * (W + 0.29)' nrd='0.29 / W' nrs='0.29 / W' sa=0 sb=0 sd=0
+ mult=1 m=1
XM14[34] vsint[34] WL VSL VSL sky130_fd_pr__special_nfet_pass_flash L=0.15 W=0.45 nf=1 ad='1 * W * 0.29'
+ as='1 * W * 0.29' pd='2 * (W + 0.29)' ps='2 * (W + 0.29)' nrd='0.29 / W' nrs='0.29 / W' sa=0 sb=0 sd=0
+ mult=1 m=1
XM14[33] vsint[33] WL VSL VSL sky130_fd_pr__special_nfet_pass_flash L=0.15 W=0.45 nf=1 ad='1 * W * 0.29'
+ as='1 * W * 0.29' pd='2 * (W + 0.29)' ps='2 * (W + 0.29)' nrd='0.29 / W' nrs='0.29 / W' sa=0 sb=0 sd=0
+ mult=1 m=1
XM14[32] vsint[32] WL VSL VSL sky130_fd_pr__special_nfet_pass_flash L=0.15 W=0.45 nf=1 ad='1 * W * 0.29'
+ as='1 * W * 0.29' pd='2 * (W + 0.29)' ps='2 * (W + 0.29)' nrd='0.29 / W' nrs='0.29 / W' sa=0 sb=0 sd=0
+ mult=1 m=1
XM14[31] vsint[31] WL VSL VSL sky130_fd_pr__special_nfet_pass_flash L=0.15 W=0.45 nf=1 ad='1 * W * 0.29'
+ as='1 * W * 0.29' pd='2 * (W + 0.29)' ps='2 * (W + 0.29)' nrd='0.29 / W' nrs='0.29 / W' sa=0 sb=0 sd=0
+ mult=1 m=1
XM14[30] vsint[30] WL VSL VSL sky130_fd_pr__special_nfet_pass_flash L=0.15 W=0.45 nf=1 ad='1 * W * 0.29'
+ as='1 * W * 0.29' pd='2 * (W + 0.29)' ps='2 * (W + 0.29)' nrd='0.29 / W' nrs='0.29 / W' sa=0 sb=0 sd=0
+ mult=1 m=1
XM14[29] vsint[29] WL VSL VSL sky130_fd_pr__special_nfet_pass_flash L=0.15 W=0.45 nf=1 ad='1 * W * 0.29'
+ as='1 * W * 0.29' pd='2 * (W + 0.29)' ps='2 * (W + 0.29)' nrd='0.29 / W' nrs='0.29 / W' sa=0 sb=0 sd=0
+ mult=1 m=1
XM14[28] vsint[28] WL VSL VSL sky130_fd_pr__special_nfet_pass_flash L=0.15 W=0.45 nf=1 ad='1 * W * 0.29'
+ as='1 * W * 0.29' pd='2 * (W + 0.29)' ps='2 * (W + 0.29)' nrd='0.29 / W' nrs='0.29 / W' sa=0 sb=0 sd=0
+ mult=1 m=1
XM14[27] vsint[27] WL VSL VSL sky130_fd_pr__special_nfet_pass_flash L=0.15 W=0.45 nf=1 ad='1 * W * 0.29'
+ as='1 * W * 0.29' pd='2 * (W + 0.29)' ps='2 * (W + 0.29)' nrd='0.29 / W' nrs='0.29 / W' sa=0 sb=0 sd=0
+ mult=1 m=1
XM14[26] vsint[26] WL VSL VSL sky130_fd_pr__special_nfet_pass_flash L=0.15 W=0.45 nf=1 ad='1 * W * 0.29'
+ as='1 * W * 0.29' pd='2 * (W + 0.29)' ps='2 * (W + 0.29)' nrd='0.29 / W' nrs='0.29 / W' sa=0 sb=0 sd=0
+ mult=1 m=1
XM14[25] vsint[25] WL VSL VSL sky130_fd_pr__special_nfet_pass_flash L=0.15 W=0.45 nf=1 ad='1 * W * 0.29'
+ as='1 * W * 0.29' pd='2 * (W + 0.29)' ps='2 * (W + 0.29)' nrd='0.29 / W' nrs='0.29 / W' sa=0 sb=0 sd=0
+ mult=1 m=1
XM14[24] vsint[24] WL VSL VSL sky130_fd_pr__special_nfet_pass_flash L=0.15 W=0.45 nf=1 ad='1 * W * 0.29'
+ as='1 * W * 0.29' pd='2 * (W + 0.29)' ps='2 * (W + 0.29)' nrd='0.29 / W' nrs='0.29 / W' sa=0 sb=0 sd=0
+ mult=1 m=1
XM14[23] vsint[23] WL VSL VSL sky130_fd_pr__special_nfet_pass_flash L=0.15 W=0.45 nf=1 ad='1 * W * 0.29'
+ as='1 * W * 0.29' pd='2 * (W + 0.29)' ps='2 * (W + 0.29)' nrd='0.29 / W' nrs='0.29 / W' sa=0 sb=0 sd=0
+ mult=1 m=1
XM14[22] vsint[22] WL VSL VSL sky130_fd_pr__special_nfet_pass_flash L=0.15 W=0.45 nf=1 ad='1 * W * 0.29'
+ as='1 * W * 0.29' pd='2 * (W + 0.29)' ps='2 * (W + 0.29)' nrd='0.29 / W' nrs='0.29 / W' sa=0 sb=0 sd=0
+ mult=1 m=1
XM14[21] vsint[21] WL VSL VSL sky130_fd_pr__special_nfet_pass_flash L=0.15 W=0.45 nf=1 ad='1 * W * 0.29'
+ as='1 * W * 0.29' pd='2 * (W + 0.29)' ps='2 * (W + 0.29)' nrd='0.29 / W' nrs='0.29 / W' sa=0 sb=0 sd=0
+ mult=1 m=1
XM14[20] vsint[20] WL VSL VSL sky130_fd_pr__special_nfet_pass_flash L=0.15 W=0.45 nf=1 ad='1 * W * 0.29'
+ as='1 * W * 0.29' pd='2 * (W + 0.29)' ps='2 * (W + 0.29)' nrd='0.29 / W' nrs='0.29 / W' sa=0 sb=0 sd=0
+ mult=1 m=1
XM14[19] vsint[19] WL VSL VSL sky130_fd_pr__special_nfet_pass_flash L=0.15 W=0.45 nf=1 ad='1 * W * 0.29'
+ as='1 * W * 0.29' pd='2 * (W + 0.29)' ps='2 * (W + 0.29)' nrd='0.29 / W' nrs='0.29 / W' sa=0 sb=0 sd=0
+ mult=1 m=1
XM14[18] vsint[18] WL VSL VSL sky130_fd_pr__special_nfet_pass_flash L=0.15 W=0.45 nf=1 ad='1 * W * 0.29'
+ as='1 * W * 0.29' pd='2 * (W + 0.29)' ps='2 * (W + 0.29)' nrd='0.29 / W' nrs='0.29 / W' sa=0 sb=0 sd=0
+ mult=1 m=1
XM14[17] vsint[17] WL VSL VSL sky130_fd_pr__special_nfet_pass_flash L=0.15 W=0.45 nf=1 ad='1 * W * 0.29'
+ as='1 * W * 0.29' pd='2 * (W + 0.29)' ps='2 * (W + 0.29)' nrd='0.29 / W' nrs='0.29 / W' sa=0 sb=0 sd=0
+ mult=1 m=1
XM14[16] vsint[16] WL VSL VSL sky130_fd_pr__special_nfet_pass_flash L=0.15 W=0.45 nf=1 ad='1 * W * 0.29'
+ as='1 * W * 0.29' pd='2 * (W + 0.29)' ps='2 * (W + 0.29)' nrd='0.29 / W' nrs='0.29 / W' sa=0 sb=0 sd=0
+ mult=1 m=1
XM14[15] vsint[15] WL VSL VSL sky130_fd_pr__special_nfet_pass_flash L=0.15 W=0.45 nf=1 ad='1 * W * 0.29'
+ as='1 * W * 0.29' pd='2 * (W + 0.29)' ps='2 * (W + 0.29)' nrd='0.29 / W' nrs='0.29 / W' sa=0 sb=0 sd=0
+ mult=1 m=1
XM14[14] vsint[14] WL VSL VSL sky130_fd_pr__special_nfet_pass_flash L=0.15 W=0.45 nf=1 ad='1 * W * 0.29'
+ as='1 * W * 0.29' pd='2 * (W + 0.29)' ps='2 * (W + 0.29)' nrd='0.29 / W' nrs='0.29 / W' sa=0 sb=0 sd=0
+ mult=1 m=1
XM14[13] vsint[13] WL VSL VSL sky130_fd_pr__special_nfet_pass_flash L=0.15 W=0.45 nf=1 ad='1 * W * 0.29'
+ as='1 * W * 0.29' pd='2 * (W + 0.29)' ps='2 * (W + 0.29)' nrd='0.29 / W' nrs='0.29 / W' sa=0 sb=0 sd=0
+ mult=1 m=1
XM14[12] vsint[12] WL VSL VSL sky130_fd_pr__special_nfet_pass_flash L=0.15 W=0.45 nf=1 ad='1 * W * 0.29'
+ as='1 * W * 0.29' pd='2 * (W + 0.29)' ps='2 * (W + 0.29)' nrd='0.29 / W' nrs='0.29 / W' sa=0 sb=0 sd=0
+ mult=1 m=1
XM14[11] vsint[11] WL VSL VSL sky130_fd_pr__special_nfet_pass_flash L=0.15 W=0.45 nf=1 ad='1 * W * 0.29'
+ as='1 * W * 0.29' pd='2 * (W + 0.29)' ps='2 * (W + 0.29)' nrd='0.29 / W' nrs='0.29 / W' sa=0 sb=0 sd=0
+ mult=1 m=1
XM14[10] vsint[10] WL VSL VSL sky130_fd_pr__special_nfet_pass_flash L=0.15 W=0.45 nf=1 ad='1 * W * 0.29'
+ as='1 * W * 0.29' pd='2 * (W + 0.29)' ps='2 * (W + 0.29)' nrd='0.29 / W' nrs='0.29 / W' sa=0 sb=0 sd=0
+ mult=1 m=1
XM14[9] vsint[9] WL VSL VSL sky130_fd_pr__special_nfet_pass_flash L=0.15 W=0.45 nf=1 ad='1 * W * 0.29'
+ as='1 * W * 0.29' pd='2 * (W + 0.29)' ps='2 * (W + 0.29)' nrd='0.29 / W' nrs='0.29 / W' sa=0 sb=0 sd=0
+ mult=1 m=1
XM14[8] vsint[8] WL VSL VSL sky130_fd_pr__special_nfet_pass_flash L=0.15 W=0.45 nf=1 ad='1 * W * 0.29'
+ as='1 * W * 0.29' pd='2 * (W + 0.29)' ps='2 * (W + 0.29)' nrd='0.29 / W' nrs='0.29 / W' sa=0 sb=0 sd=0
+ mult=1 m=1
XM14[7] vsint[7] WL VSL VSL sky130_fd_pr__special_nfet_pass_flash L=0.15 W=0.45 nf=1 ad='1 * W * 0.29'
+ as='1 * W * 0.29' pd='2 * (W + 0.29)' ps='2 * (W + 0.29)' nrd='0.29 / W' nrs='0.29 / W' sa=0 sb=0 sd=0
+ mult=1 m=1
XM14[6] vsint[6] WL VSL VSL sky130_fd_pr__special_nfet_pass_flash L=0.15 W=0.45 nf=1 ad='1 * W * 0.29'
+ as='1 * W * 0.29' pd='2 * (W + 0.29)' ps='2 * (W + 0.29)' nrd='0.29 / W' nrs='0.29 / W' sa=0 sb=0 sd=0
+ mult=1 m=1
XM14[5] vsint[5] WL VSL VSL sky130_fd_pr__special_nfet_pass_flash L=0.15 W=0.45 nf=1 ad='1 * W * 0.29'
+ as='1 * W * 0.29' pd='2 * (W + 0.29)' ps='2 * (W + 0.29)' nrd='0.29 / W' nrs='0.29 / W' sa=0 sb=0 sd=0
+ mult=1 m=1
XM14[4] vsint[4] WL VSL VSL sky130_fd_pr__special_nfet_pass_flash L=0.15 W=0.45 nf=1 ad='1 * W * 0.29'
+ as='1 * W * 0.29' pd='2 * (W + 0.29)' ps='2 * (W + 0.29)' nrd='0.29 / W' nrs='0.29 / W' sa=0 sb=0 sd=0
+ mult=1 m=1
XM14[3] vsint[3] WL VSL VSL sky130_fd_pr__special_nfet_pass_flash L=0.15 W=0.45 nf=1 ad='1 * W * 0.29'
+ as='1 * W * 0.29' pd='2 * (W + 0.29)' ps='2 * (W + 0.29)' nrd='0.29 / W' nrs='0.29 / W' sa=0 sb=0 sd=0
+ mult=1 m=1
XM14[2] vsint[2] WL VSL VSL sky130_fd_pr__special_nfet_pass_flash L=0.15 W=0.45 nf=1 ad='1 * W * 0.29'
+ as='1 * W * 0.29' pd='2 * (W + 0.29)' ps='2 * (W + 0.29)' nrd='0.29 / W' nrs='0.29 / W' sa=0 sb=0 sd=0
+ mult=1 m=1
XM14[1] vsint[1] WL VSL VSL sky130_fd_pr__special_nfet_pass_flash L=0.15 W=0.45 nf=1 ad='1 * W * 0.29'
+ as='1 * W * 0.29' pd='2 * (W + 0.29)' ps='2 * (W + 0.29)' nrd='0.29 / W' nrs='0.29 / W' sa=0 sb=0 sd=0
+ mult=1 m=1
XM14[0] vsint[0] WL VSL VSL sky130_fd_pr__special_nfet_pass_flash L=0.15 W=0.45 nf=1 ad='1 * W * 0.29'
+ as='1 * W * 0.29' pd='2 * (W + 0.29)' ps='2 * (W + 0.29)' nrd='0.29 / W' nrs='0.29 / W' sa=0 sb=0 sd=0
+ mult=1 m=1
XM15[63] net4 wls_x vsint[63] VSL sky130_fd_bs_flash__special_sonosfet_star L=0.22 W=0.45 nf=1 ad='1 * W * 0.29'
+ as='1 * W * 0.29' pd='2 * (W + 0.29)' ps='2 * (W + 0.29)' nrd='0.29 / W' nrs='0.29 / W' sa=0 sb=0 sd=0
+ mult=1 m=1
XM14[63] vsint[63] WL VSL VSL sky130_fd_pr__special_nfet_pass_flash L=0.15 W=0.45 nf=1 ad='1 * W * 0.29'
+ as='1 * W * 0.29' pd='2 * (W + 0.29)' ps='2 * (W + 0.29)' nrd='0.29 / W' nrs='0.29 / W' sa=0 sb=0 sd=0
+ mult=1 m=1
Vmeas1[62] VBL net3[62] 0
Vmeas1[61] VBL net3[61] 0
Vmeas1[60] VBL net3[60] 0
Vmeas1[59] VBL net3[59] 0
Vmeas1[58] VBL net3[58] 0
Vmeas1[57] VBL net3[57] 0
Vmeas1[56] VBL net3[56] 0
Vmeas1[55] VBL net3[55] 0
Vmeas1[54] VBL net3[54] 0
Vmeas1[53] VBL net3[53] 0
Vmeas1[52] VBL net3[52] 0
Vmeas1[51] VBL net3[51] 0
Vmeas1[50] VBL net3[50] 0
Vmeas1[49] VBL net3[49] 0
Vmeas1[48] VBL net3[48] 0
Vmeas1[47] VBL net3[47] 0
Vmeas1[46] VBL net3[46] 0
Vmeas1[45] VBL net3[45] 0
Vmeas1[44] VBL net3[44] 0
Vmeas1[43] VBL net3[43] 0
Vmeas1[42] VBL net3[42] 0
Vmeas1[41] VBL net3[41] 0
Vmeas1[40] VBL net3[40] 0
Vmeas1[39] VBL net3[39] 0
Vmeas1[38] VBL net3[38] 0
Vmeas1[37] VBL net3[37] 0
Vmeas1[36] VBL net3[36] 0
Vmeas1[35] VBL net3[35] 0
Vmeas1[34] VBL net3[34] 0
Vmeas1[33] VBL net3[33] 0
Vmeas1[32] VBL net3[32] 0
Vmeas1[31] VBL net3[31] 0
Vmeas1[30] VBL net3[30] 0
Vmeas1[29] VBL net3[29] 0
Vmeas1[28] VBL net3[28] 0
Vmeas1[27] VBL net3[27] 0
Vmeas1[26] VBL net3[26] 0
Vmeas1[25] VBL net3[25] 0
Vmeas1[24] VBL net3[24] 0
Vmeas1[23] VBL net3[23] 0
Vmeas1[22] VBL net3[22] 0
Vmeas1[21] VBL net3[21] 0
Vmeas1[20] VBL net3[20] 0
Vmeas1[19] VBL net3[19] 0
Vmeas1[18] VBL net3[18] 0
Vmeas1[17] VBL net3[17] 0
Vmeas1[16] VBL net3[16] 0
Vmeas1[15] VBL net3[15] 0
Vmeas1[14] VBL net3[14] 0
Vmeas1[13] VBL net3[13] 0
Vmeas1[12] VBL net3[12] 0
Vmeas1[11] VBL net3[11] 0
Vmeas1[10] VBL net3[10] 0
Vmeas1[9] VBL net3[9] 0
Vmeas1[8] VBL net3[8] 0
Vmeas1[7] VBL net3[7] 0
Vmeas1[6] VBL net3[6] 0
Vmeas1[5] VBL net3[5] 0
Vmeas1[4] VBL net3[4] 0
Vmeas1[3] VBL net3[3] 0
Vmeas1[2] VBL net3[2] 0
Vmeas1[1] VBL net3[1] 0
Vmeas1[0] VBL net3[0] 0
.save i(vmeas1[62])
.save i(vmeas1[61])
.save i(vmeas1[60])
.save i(vmeas1[59])
.save i(vmeas1[58])
.save i(vmeas1[57])
.save i(vmeas1[56])
.save i(vmeas1[55])
.save i(vmeas1[54])
.save i(vmeas1[53])
.save i(vmeas1[52])
.save i(vmeas1[51])
.save i(vmeas1[50])
.save i(vmeas1[49])
.save i(vmeas1[48])
.save i(vmeas1[47])
.save i(vmeas1[46])
.save i(vmeas1[45])
.save i(vmeas1[44])
.save i(vmeas1[43])
.save i(vmeas1[42])
.save i(vmeas1[41])
.save i(vmeas1[40])
.save i(vmeas1[39])
.save i(vmeas1[38])
.save i(vmeas1[37])
.save i(vmeas1[36])
.save i(vmeas1[35])
.save i(vmeas1[34])
.save i(vmeas1[33])
.save i(vmeas1[32])
.save i(vmeas1[31])
.save i(vmeas1[30])
.save i(vmeas1[29])
.save i(vmeas1[28])
.save i(vmeas1[27])
.save i(vmeas1[26])
.save i(vmeas1[25])
.save i(vmeas1[24])
.save i(vmeas1[23])
.save i(vmeas1[22])
.save i(vmeas1[21])
.save i(vmeas1[20])
.save i(vmeas1[19])
.save i(vmeas1[18])
.save i(vmeas1[17])
.save i(vmeas1[16])
.save i(vmeas1[15])
.save i(vmeas1[14])
.save i(vmeas1[13])
.save i(vmeas1[12])
.save i(vmeas1[11])
.save i(vmeas1[10])
.save i(vmeas1[9])
.save i(vmeas1[8])
.save i(vmeas1[7])
.save i(vmeas1[6])
.save i(vmeas1[5])
.save i(vmeas1[4])
.save i(vmeas1[3])
.save i(vmeas1[2])
.save i(vmeas1[1])
.save i(vmeas1[0])
Vmeas2 VBL net4 0
.save i(vmeas2)
**** begin user architecture code


.param VDD=1.8
.param VPCX=6.7
.param VGCX=-3.8
.option savecurrents
.control
  unset appendwrite
  save all
  op
  remzerovec
  write test_rowdv_2t.raw
  *set appendwrite

  tran 1n 1.6u
  remzerovec
  write test_rowdv_2t.raw
.endc



** opencircuitdesign pdks install
.lib $::SKYWATER_MODELS/sky130.lib.spice tt
.include $::SKYWATER_MODELS/sonos_e/begin_of_life.spice
.include $::SKYWATER_MODELS/sonos_e/begin_of_life.pm3.spice
.include $::SKYWATER_MODELS/sonos_p/begin_of_life.spice
.include $::SKYWATER_MODELS/sonos_p/begin_of_life.pm3.spice
* .include
*+ $::SKYWATER_MODELS/../../libs.ref/sky130_fd_pr/spice/sky130_fd_pr__special_nfet_pass_flash.pm3.spice

**** end user architecture code
**.ends

* expanding   symbol:  rowdv_2t.sym # of pins=14
** sym_path: integrated/rowdv_2t_sonos/rowdv_2t.sym
** sch_path: integrated/rowdv_2t_sonos/rowdv_2t.sch
.subckt rowdv_2t ssect_vpc en_vdd enb_vdd p_vpc p_vdd pb_vdd swgnd VPC VGC VDD VSS VSUBS WLS WL
*.ipin p_vpc
*.opin WLS
*.ipin swgnd
*.ipin VDD
*.ipin VSS
*.ipin en_vdd
*.ipin enb_vdd
*.ipin VGC
*.ipin VPC
*.ipin ssect_vpc
*.opin WL
*.ipin VSUBS
*.ipin p_vdd
*.ipin pb_vdd
XM1 wlsx p_vdd swgnd VSUBS sky130_fd_pr__nfet_g5v0d10v5 L=0.5 W=1 nf=1 ad='int((nf+1)/2) * W/nf * 0.29'
+ as='int((nf+2)/2) * W/nf * 0.29' pd='2*int((nf+1)/2) * (W/nf + 0.29)' ps='2*int((nf+2)/2) * (W/nf + 0.29)'
+ nrd='0.29 / W' nrs='0.29 / W' sa=0 sb=0 sd=0 mult=1 m=1
XM2 pbs p_vpc VPC VPC sky130_fd_pr__pfet_g5v0d10v5 L=0.5 W=1 nf=1 ad='int((nf+1)/2) * W/nf * 0.29' as='int((nf+2)/2) * W/nf * 0.29'
+ pd='2*int((nf+1)/2) * (W/nf + 0.29)' ps='2*int((nf+2)/2) * (W/nf + 0.29)' nrd='0.29 / W' nrs='0.29 / W'
+ sa=0 sb=0 sd=0 mult=1 m=1
XM3 wlsy pb_vdd VGC VGC sky130_fd_pr__nfet_g5v0d10v5 L=0.5 W=5 nf=1 ad='int((nf+1)/2) * W/nf * 0.29'
+ as='int((nf+2)/2) * W/nf * 0.29' pd='2*int((nf+1)/2) * (W/nf + 0.29)' ps='2*int((nf+2)/2) * (W/nf + 0.29)'
+ nrd='0.29 / W' nrs='0.29 / W' sa=0 sb=0 sd=0 mult=1 m=1
XM4 WLS pbs VPC VPC sky130_fd_pr__pfet_g5v0d10v5 L=0.5 W=5 nf=1 ad='int((nf+1)/2) * W/nf * 0.29' as='int((nf+2)/2) * W/nf * 0.29'
+ pd='2*int((nf+1)/2) * (W/nf + 0.29)' ps='2*int((nf+2)/2) * (W/nf + 0.29)' nrd='0.29 / W' nrs='0.29 / W'
+ sa=0 sb=0 sd=0 mult=1 m=1
XM6 pbpass p_vpc VDD VDD sky130_fd_pr__pfet_g5v0d10v5 L=0.5 W=1 nf=1 ad='int((nf+1)/2) * W/nf * 0.29'
+ as='int((nf+2)/2) * W/nf * 0.29' pd='2*int((nf+1)/2) * (W/nf + 0.29)' ps='2*int((nf+2)/2) * (W/nf + 0.29)'
+ nrd='0.29 / W' nrs='0.29 / W' sa=0 sb=0 sd=0 mult=1 m=1
XM7 wlil pbpass VSS VSUBS sky130_fd_pr__nfet_g5v0d10v5 L=0.5 W=5 nf=1 ad='int((nf+1)/2) * W/nf * 0.29'
+ as='int((nf+2)/2) * W/nf * 0.29' pd='2*int((nf+1)/2) * (W/nf + 0.29)' ps='2*int((nf+2)/2) * (W/nf + 0.29)'
+ nrd='0.29 / W' nrs='0.29 / W' sa=0 sb=0 sd=0 mult=1 m=1
XM9 WL en_vdd wlih VDD sky130_fd_pr__pfet_g5v0d10v5 L=0.5 W=10 nf=1 ad='int((nf+1)/2) * W/nf * 0.29'
+ as='int((nf+2)/2) * W/nf * 0.29' pd='2*int((nf+1)/2) * (W/nf + 0.29)' ps='2*int((nf+2)/2) * (W/nf + 0.29)'
+ nrd='0.29 / W' nrs='0.29 / W' sa=0 sb=0 sd=0 mult=1 m=1
XM8 WL enb_vdd wlil VSUBS sky130_fd_pr__nfet_g5v0d10v5 L=0.5 W=5 nf=1 ad='int((nf+1)/2) * W/nf * 0.29'
+ as='int((nf+2)/2) * W/nf * 0.29' pd='2*int((nf+1)/2) * (W/nf + 0.29)' ps='2*int((nf+2)/2) * (W/nf + 0.29)'
+ nrd='0.29 / W' nrs='0.29 / W' sa=0 sb=0 sd=0 mult=1 m=1
XM10 wlih pbpass VDD VDD sky130_fd_pr__pfet_g5v0d10v5 L=0.5 W=10 nf=1 ad='int((nf+1)/2) * W/nf * 0.29'
+ as='int((nf+2)/2) * W/nf * 0.29' pd='2*int((nf+1)/2) * (W/nf + 0.29)' ps='2*int((nf+2)/2) * (W/nf + 0.29)'
+ nrd='0.29 / W' nrs='0.29 / W' sa=0 sb=0 sd=0 mult=1 m=1
XM11 pbs ssect_vpc VPC VPC sky130_fd_pr__pfet_g5v0d10v5 L=0.5 W=1 nf=1 ad='int((nf+1)/2) * W/nf * 0.29'
+ as='int((nf+2)/2) * W/nf * 0.29' pd='2*int((nf+1)/2) * (W/nf + 0.29)' ps='2*int((nf+2)/2) * (W/nf + 0.29)'
+ nrd='0.29 / W' nrs='0.29 / W' sa=0 sb=0 sd=0 mult=1 m=1
XM5 pbpass p_vdd VSS VSS sky130_fd_pr__nfet_g5v0d10v5 L=0.5 W=1 nf=1 ad='int((nf+1)/2) * W/nf * 0.29'
+ as='int((nf+2)/2) * W/nf * 0.29' pd='2*int((nf+1)/2) * (W/nf + 0.29)' ps='2*int((nf+2)/2) * (W/nf + 0.29)'
+ nrd='0.29 / W' nrs='0.29 / W' sa=0 sb=0 sd=0 mult=1 m=1
XM1x pbs VDD wlsx VSUBS sky130_fd_pr__nfet_g5v0d10v5 L=0.5 W=1 nf=1 ad='int((nf+1)/2) * W/nf * 0.29'
+ as='int((nf+2)/2) * W/nf * 0.29' pd='2*int((nf+1)/2) * (W/nf + 0.29)' ps='2*int((nf+2)/2) * (W/nf + 0.29)'
+ nrd='0.29 / W' nrs='0.29 / W' sa=0 sb=0 sd=0 mult=1 m=1
XM3x WLS VDD wlsy VGC sky130_fd_pr__nfet_g5v0d10v5 L=0.5 W=5 nf=1 ad='int((nf+1)/2) * W/nf * 0.29' as='int((nf+2)/2) * W/nf * 0.29'
+ pd='2*int((nf+1)/2) * (W/nf + 0.29)' ps='2*int((nf+2)/2) * (W/nf + 0.29)' nrd='0.29 / W' nrs='0.29 / W'
+ sa=0 sb=0 sd=0 mult=1 m=1
.ends

.GLOBAL GND
.end
